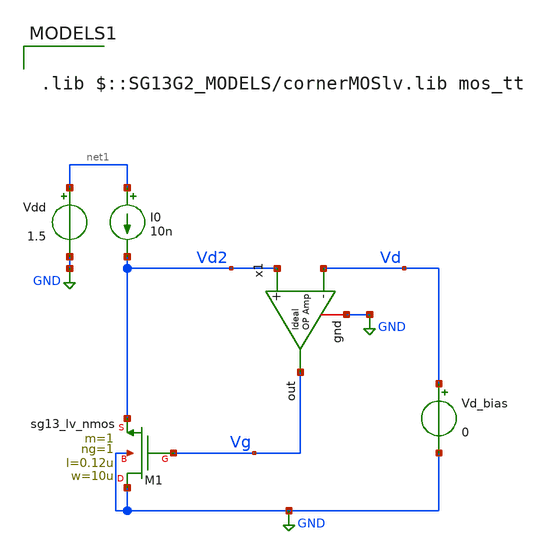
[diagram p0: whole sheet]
** sch_path: ihp_tutorials/Extraction/nmos_sigma_ext.sch
**.subckt nmos_sigma_ext
x1 Vg Vd2 Vd GND ampOp_ideal
I0 net1 Vd2 10n
Vd_bias Vd GND 0
Vdd net1 GND 1.5
XM1 GND Vg Vd2 GND sg13_lv_nmos w=10u l=0.12u ng=1 m=1 mm_ok=1
**** begin user architecture code



.option gmin = 1e-18

.nodeset V(vd2)=1.5

.control
pre_osdi ./psp103_nqs.osdi
save all

dc Vd_bias  0.05 1.5 25.9m

let vd_interp = 1.5/3
let sigma = -deriv(V(vg))/deriv(V(vd))
save sigma

echo
echo
echo


echo Sigma @ VD=$&vd_interp:
meas dc sigma_value FIND sigma WHEN V(vd)=vd_interp

echo
echo
echo
write nmos_sigma_ext.raw

.endc





.lib $::SG13G2_MODELS/cornerMOSlv.lib mos_tt

**** end user architecture code
**.ends

* expanding   symbol:  /home/gmaranhao/Desktop/gf180_work/auxLib/ampOp_ideal.sym # of pins=4
** sym_path: gf_tutorials/auxLib/ampOp_ideal.sym
** sch_path: gf_tutorials/auxLib/ampOp_ideal.sch
.subckt ampOp_ideal out + - gnd
*.ipin +
*.ipin -
*.opin out
*.iopin gnd
E1 out gnd + - 10000000
.ends

.GLOBAL GND
.end
